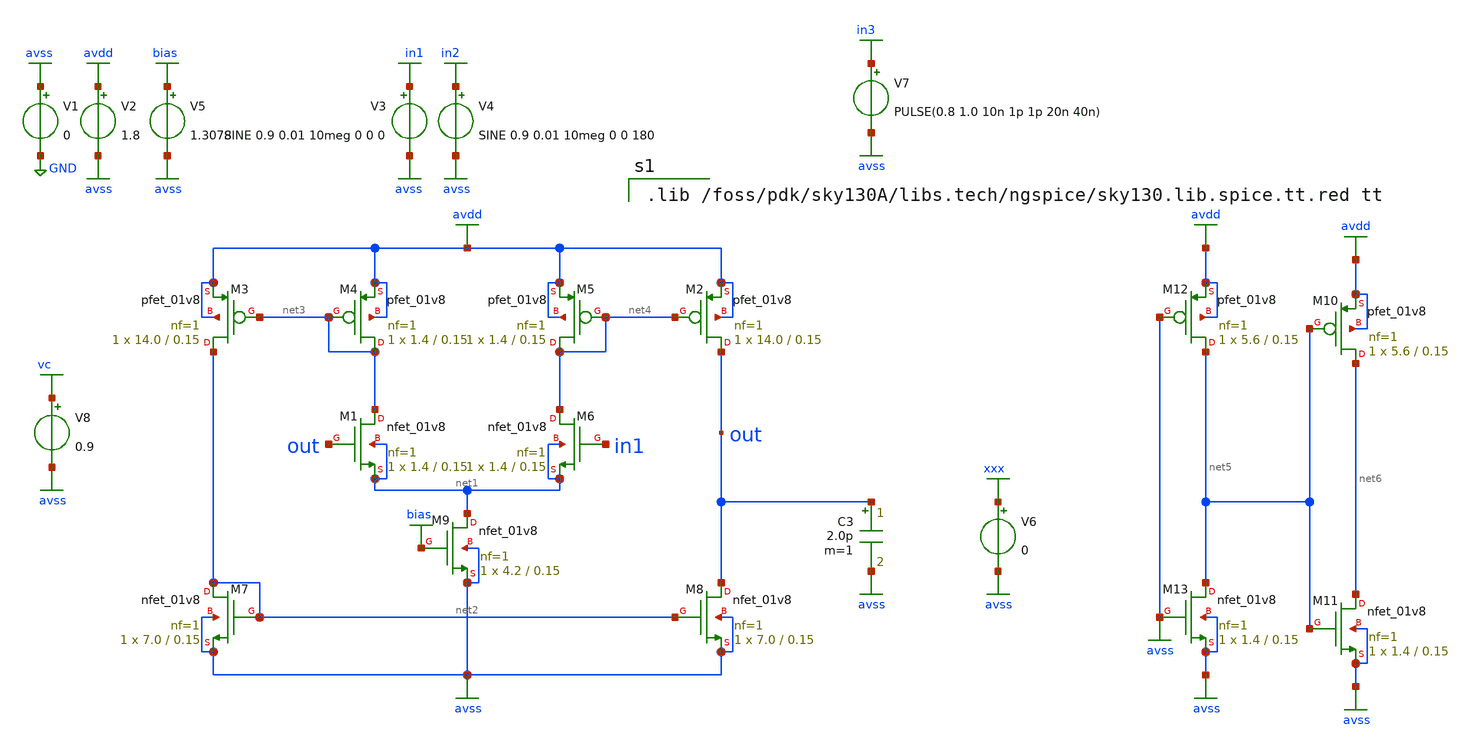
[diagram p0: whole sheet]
** sch_path: xschem/ota_2_sim.sch
**.subckt ota_2_sim
XM1 net3 out net1 net1 sky130_fd_pr__nfet_01v8 L=0.15 W=1.4 nf=1 ad='int((nf+1)/2) * W/nf * 0.29' as='int((nf+2)/2) * W/nf * 0.29'
+ pd='2*int((nf+1)/2) * (W/nf + 0.29)' ps='2*int((nf+2)/2) * (W/nf + 0.29)' nrd='0.29 / W' nrs='0.29 / W'
+ sa=0 sb=0 sd=0 mult=1 m=1
XM3 net2 net3 avdd avdd sky130_fd_pr__pfet_01v8 L=0.15 W=14.0 nf=1 ad='int((nf+1)/2) * W/nf * 0.29' as='int((nf+2)/2) * W/nf * 0.29'
+ pd='2*int((nf+1)/2) * (W/nf + 0.29)' ps='2*int((nf+2)/2) * (W/nf + 0.29)' nrd='0.29 / W' nrs='0.29 / W'
+ sa=0 sb=0 sd=0 mult=1 m=1
XM2 out net4 avdd avdd sky130_fd_pr__pfet_01v8 L=0.15 W=14.0 nf=1 ad='int((nf+1)/2) * W/nf * 0.29' as='int((nf+2)/2) * W/nf * 0.29'
+ pd='2*int((nf+1)/2) * (W/nf + 0.29)' ps='2*int((nf+2)/2) * (W/nf + 0.29)' nrd='0.29 / W' nrs='0.29 / W'
+ sa=0 sb=0 sd=0 mult=1 m=1
XM6 net4 in1 net1 net1 sky130_fd_pr__nfet_01v8 L=0.15 W=1.4 nf=1 ad='int((nf+1)/2) * W/nf * 0.29' as='int((nf+2)/2) * W/nf * 0.29'
+ pd='2*int((nf+1)/2) * (W/nf + 0.29)' ps='2*int((nf+2)/2) * (W/nf + 0.29)' nrd='0.29 / W' nrs='0.29 / W'
+ sa=0 sb=0 sd=0 mult=1 m=1
XM7 net2 net2 avss avss sky130_fd_pr__nfet_01v8 L=0.15 W=7.0 nf=1 ad='int((nf+1)/2) * W/nf * 0.29' as='int((nf+2)/2) * W/nf * 0.29'
+ pd='2*int((nf+1)/2) * (W/nf + 0.29)' ps='2*int((nf+2)/2) * (W/nf + 0.29)' nrd='0.29 / W' nrs='0.29 / W'
+ sa=0 sb=0 sd=0 mult=1 m=1
XM8 out net2 avss avss sky130_fd_pr__nfet_01v8 L=0.15 W=7.0 nf=1 ad='int((nf+1)/2) * W/nf * 0.29' as='int((nf+2)/2) * W/nf * 0.29'
+ pd='2*int((nf+1)/2) * (W/nf + 0.29)' ps='2*int((nf+2)/2) * (W/nf + 0.29)' nrd='0.29 / W' nrs='0.29 / W'
+ sa=0 sb=0 sd=0 mult=1 m=1
V1 avss GND 0
V2 avdd avss 1.8
V4 in2 avss SINE 0.9 0.01 10meg 0 0 180
V3 in1 avss SINE 0.9 0.01 10meg 0 0 0
C3 out avss 2.0p m=1
V5 bias avss 1.3078
XM4 net3 net3 avdd avdd sky130_fd_pr__pfet_01v8 L=0.15 W=1.4 nf=1 ad='int((nf+1)/2) * W/nf * 0.29' as='int((nf+2)/2) * W/nf * 0.29'
+ pd='2*int((nf+1)/2) * (W/nf + 0.29)' ps='2*int((nf+2)/2) * (W/nf + 0.29)' nrd='0.29 / W' nrs='0.29 / W'
+ sa=0 sb=0 sd=0 mult=1 m=1
XM5 net4 net4 avdd avdd sky130_fd_pr__pfet_01v8 L=0.15 W=1.4 nf=1 ad='int((nf+1)/2) * W/nf * 0.29' as='int((nf+2)/2) * W/nf * 0.29'
+ pd='2*int((nf+1)/2) * (W/nf + 0.29)' ps='2*int((nf+2)/2) * (W/nf + 0.29)' nrd='0.29 / W' nrs='0.29 / W'
+ sa=0 sb=0 sd=0 mult=1 m=1
XM9 net1 bias avss avss sky130_fd_pr__nfet_01v8 L=0.15 W=4.2 nf=1 ad='int((nf+1)/2) * W/nf * 0.29' as='int((nf+2)/2) * W/nf * 0.29'
+ pd='2*int((nf+1)/2) * (W/nf + 0.29)' ps='2*int((nf+2)/2) * (W/nf + 0.29)' nrd='0.29 / W' nrs='0.29 / W'
+ sa=0 sb=0 sd=0 mult=1 m=1
XM12 net5 avss avdd avdd sky130_fd_pr__pfet_01v8 L=0.15 W=5.6 nf=1 ad='int((nf+1)/2) * W/nf * 0.29' as='int((nf+2)/2) * W/nf * 0.29'
+ pd='2*int((nf+1)/2) * (W/nf + 0.29)' ps='2*int((nf+2)/2) * (W/nf + 0.29)' nrd='0.29 / W' nrs='0.29 / W'
+ sa=0 sb=0 sd=0 mult=1 m=1
XM13 net5 avss avss avss sky130_fd_pr__nfet_01v8 L=0.15 W=1.4 nf=1 ad='int((nf+1)/2) * W/nf * 0.29' as='int((nf+2)/2) * W/nf * 0.29'
+ pd='2*int((nf+1)/2) * (W/nf + 0.29)' ps='2*int((nf+2)/2) * (W/nf + 0.29)' nrd='0.29 / W' nrs='0.29 / W'
+ sa=0 sb=0 sd=0 mult=1 m=1
XM10 net6 net5 avdd avdd sky130_fd_pr__pfet_01v8 L=0.15 W=5.6 nf=1 ad='int((nf+1)/2) * W/nf * 0.29' as='int((nf+2)/2) * W/nf * 0.29'
+ pd='2*int((nf+1)/2) * (W/nf + 0.29)' ps='2*int((nf+2)/2) * (W/nf + 0.29)' nrd='0.29 / W' nrs='0.29 / W'
+ sa=0 sb=0 sd=0 mult=1 m=1
XM11 net6 net5 avss avss sky130_fd_pr__nfet_01v8 L=0.15 W=1.4 nf=1 ad='int((nf+1)/2) * W/nf * 0.29' as='int((nf+2)/2) * W/nf * 0.29'
+ pd='2*int((nf+1)/2) * (W/nf + 0.29)' ps='2*int((nf+2)/2) * (W/nf + 0.29)' nrd='0.29 / W' nrs='0.29 / W'
+ sa=0 sb=0 sd=0 mult=1 m=1
V6 xxx avss 0
V7 in3 avss PULSE(0.8 1.0 10n 1p 1p 20n 40n)
V8 vc avss 0.9
**** begin user architecture code

.lib /foss/pdk/sky130A/libs.tech/ngspice/sky130.lib.spice.tt.red tt



.control
set temp=25
save in1 in2 in3 out @V1[i] @V6[i] @C3[i]
tran 0.05n 300n 0.0n
*ac dec 10 10 10meg
*plot @V1[i]
*plot in1 in2 out
*plot @V6[i]
*plot in3 out
plot in1 out
plot @C3[i]
*fft in1 in2 out
*plot db(mag(out1)) xlimit 0.1g 15g ylimit 0.0 -200
*plot db(mag(clkin)) xlimit 0.1g 15g ylimit 0.0 -200
*plot db(mag(clkin)) db(mag(out1)) db(mag(out2)) db(mag(out3)) db(mag(out4)) xlimit 0.1g 10g ylimit
*+ 0.0 -200
*compose values start=0.001 stop=0.101 step=0.01
*foreach val $&values
*	echo run = $val
*	alter @v3[sine] = [ 0.9 $val 10meg 0 0 180 ] $ vector
*	alter @v4[sine] = [ 0.9 $val 10meg 0 0 0 ] $ vector
*	save in1 in2 in3 @V6[i] @C3[i]
*	tran 0.5n 400n 10n
*	run
*end
*compose values start=0.1meg stop=1.51meg step=0.1meg
*foreach val $&values
*	echo run = $val
*	alter @v3[sine] = [ 0.9 0.01 $val 0 0 180 ] $ vector
*	alter @v4[sine] = [ 0.9 0.01 $val 0 0 0 ] $ vector
*	save in1 in2 @V6[i] out
*	tran 10n 10000n 10n
*	run
*end
*compose values start=0.85 stop=0.95 step=0.01
*foreach val $&values
*	echo run = $val
*	alter @v3[sine] = [ $val 0.01 10meg 0 0 180 ] $ vector
*	alter @v4[sine] = [ $val 0.01 10meg 0 0 0 ] $ vector
*	save in1 in2 @V6[i] out @C3[i]
*	tran 0.1n 200n 20n
*	run
*end
*plot tran1.in1 tran2.in1 tran3.in1 tran4.in1 tran5.in1 tran6.in1 tran7.in1 tran8.in1 tran9.in1
*+ tran10.in1 tran11.in1
*plot tran1.@V6[i] tran2.@V6[i] tran3.@V6[i] tran4.@V6[i] tran5.@V6[i] tran6.@V6[i] tran7.@V6[i]
*+ tran8.@V6[i] tran9.@V6[i] tran10.@V6[i] tran11.@V6[i]
*plot tran1.@C3[i] tran2.@C3[i] tran3.@C3[i] tran4.@C3[i] tran5.@C3[i] tran6.@C3[i] tran7.@C3[i]
*+ tran8.@C3[i] tran9.@C3[i] tran10.@C3[i] tran11.@C3[i]
*plot tran1.out tran2.out tran3.out tran4.out tran5.out tran6.out tran7.out tran8.out tran9.out
*+ tran10.out tran11.out
*plot tran1.out tran1.in1 tran11.out tran11.in1
*plot tran1.in1 tran1.in2 tran1.out
*plot tran1.in3 tran1.out
.endc
.end


**** end user architecture code
**.ends
.GLOBAL avdd
.GLOBAL avss
.GLOBAL GND
.GLOBAL in2
.GLOBAL bias
.GLOBAL in1
.GLOBAL xxx
.GLOBAL in3
.GLOBAL vc
.end
